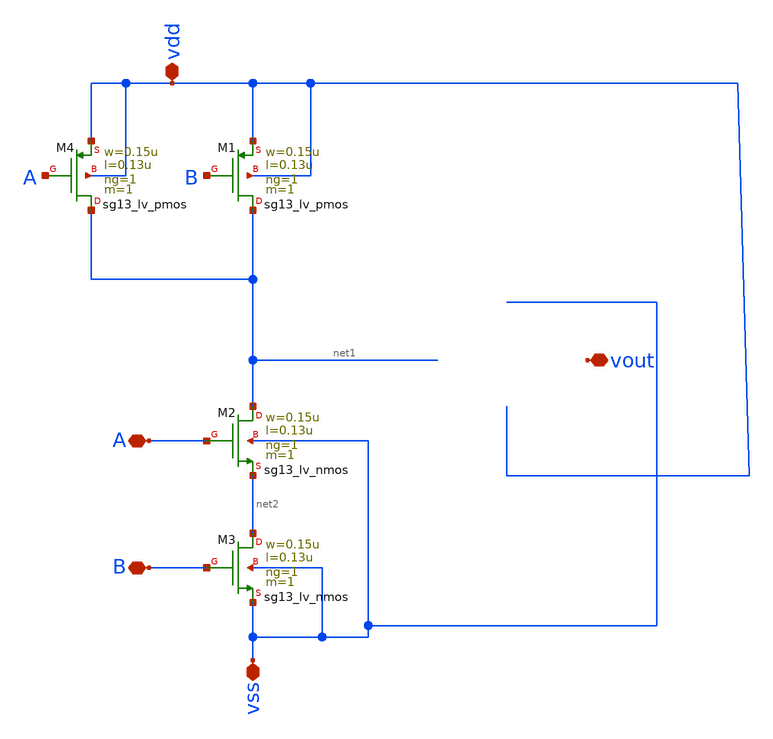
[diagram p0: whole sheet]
** sch_path: design/blocks/puertand/puertanand.sch
**.subckt puertanand A B vdd vss vout
*.iopin A
*.iopin B
*.iopin vdd
*.iopin vss
*.iopin vout
XM1 net1 B vdd vdd sg13_lv_pmos w=0.15u l=0.13u ng=1 m=1 mm_ok=1
XM2 net1 A net2 vss sg13_lv_nmos w=0.15u l=0.13u ng=1 m=1 mm_ok=1
XM3 net2 B vss vss sg13_lv_nmos w=0.15u l=0.13u ng=1 m=1 mm_ok=1
XM4 net1 A vdd vdd sg13_lv_pmos w=0.15u l=0.13u ng=1 m=1 mm_ok=1
**.ends
.end
